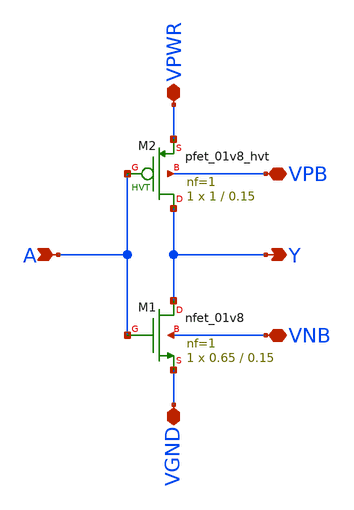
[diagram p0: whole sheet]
** sch_path: _tests/23/sky130A/inv.sch
**.subckt inv A Y VPWR VGND VPB VNB
*.ipin A
*.opin Y
*.iopin VPWR
*.iopin VGND
*.iopin VPB
*.iopin VNB
XM1 Y A VGND VNB sky130_fd_pr__nfet_01v8 L=0.15 W=0.65 nf=1 ad='int((1 + 1)/2) * 0.65 / 1 * 0.29' as='int((1 + 2)/2) * 0.65 / 1 * 0.29'
+ pd='2*int((1 + 1)/2) * (0.65 / 1 + 0.29)' ps='2*int((1 + 2)/2) * (0.65 / 1 + 0.29)' nrd='0.29 / 0.65 '
+ nrs='0.29 / 0.65 ' sa=0 sb=0 sd=0 mult=1 m=1
XM2 Y A VPWR VPB sky130_fd_pr__pfet_01v8_hvt L=0.15 W=1 nf=1 ad='int((1 + 1)/2) * 1 / 1 * 0.29' as='int((1 + 2)/2) * 1 / 1 * 0.29'
+ pd='2*int((1 + 1)/2) * (1 / 1 + 0.29)' ps='2*int((1 + 2)/2) * (1 / 1 + 0.29)' nrd='0.29 / 1 ' nrs='0.29 / 1 '
+ sa=0 sb=0 sd=0 mult=1 m=1
**.ends
.end
